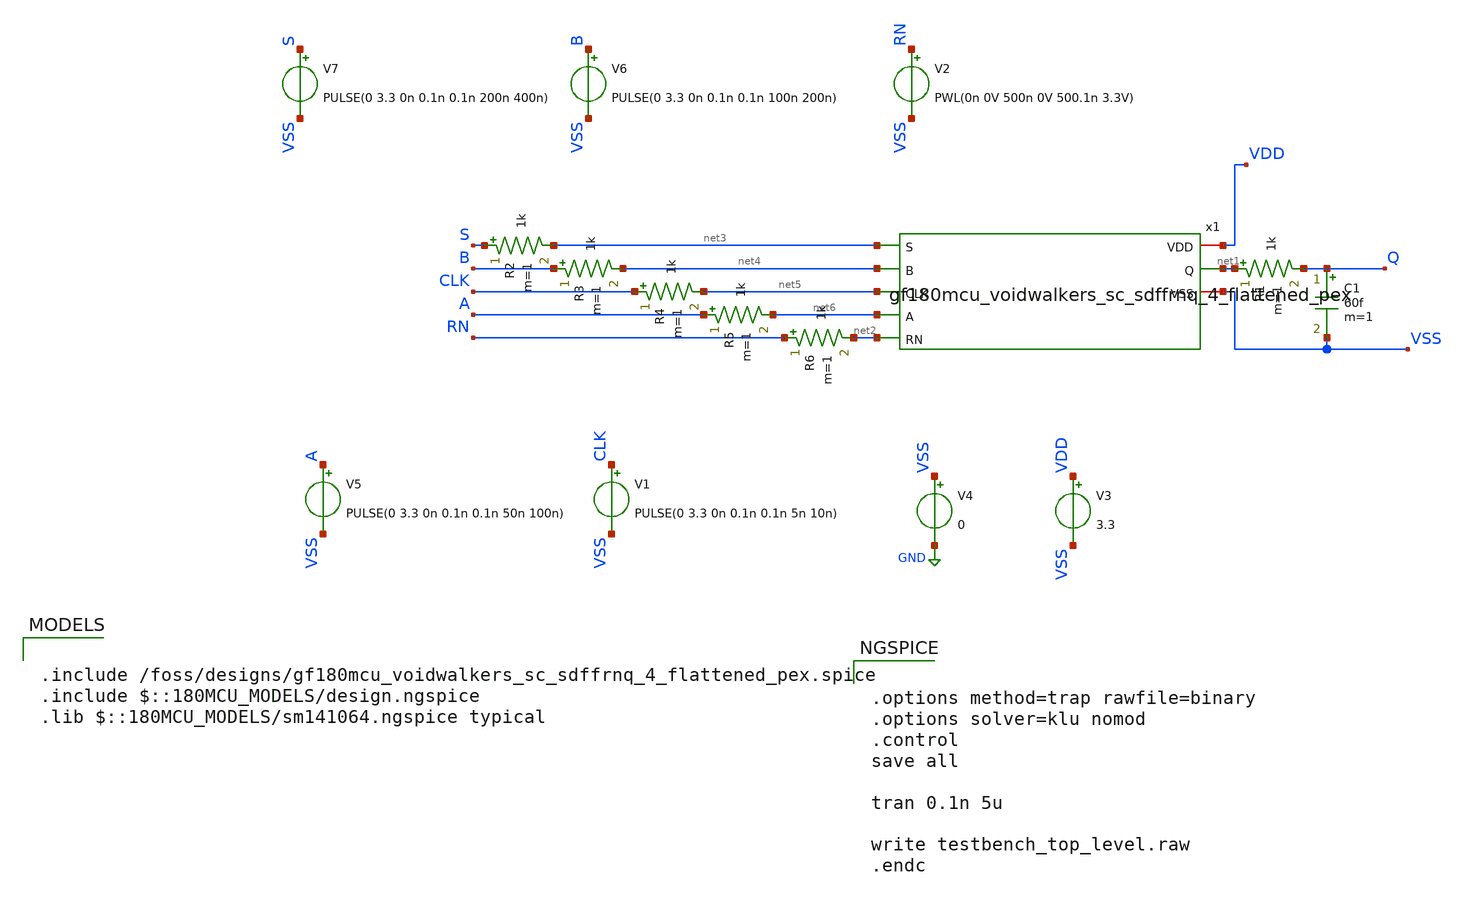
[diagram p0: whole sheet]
** sch_path: designs/libs/tb_digital/tb_toplevel/testbench_sdffrq_mux_tg.sch
**.subckt testbench_sdffrq_mux_tg
V1 CLK VSS PULSE(0 3.3 0n 0.1n 0.1n 5n 10n)
V3 VDD VSS 3.3
V4 VSS GND 0
V5 A VSS PULSE(0 3.3 0n 0.1n 0.1n 50n 100n)
V6 B VSS PULSE(0 3.3 0n 0.1n 0.1n 100n 200n)
V7 S VSS PULSE(0 3.3 0n 0.1n 0.1n 200n 400n)
V2 RN VSS PWL(0n 0V 500n 0V 500.1n 3.3V)
R1 net1 Q 1k m=1
R2 S net3 1k m=1
R3 B net4 1k m=1
R4 CLK net5 1k m=1
R5 A net6 1k m=1
R6 RN net2 1k m=1
x1 VDD VSS net6 net4 net3 net5 net2 net1 gf180mcu_voidwalkers_sc_sdffrnq_4_flattened_pex
C1 Q VSS 60f m=1
**** begin user architecture code

.include /foss/designs/gf180mcu_voidwalkers_sc_sdffrnq_4_flattened_pex.spice
.include $::180MCU_MODELS/design.ngspice
.lib $::180MCU_MODELS/sm141064.ngspice typical



.options method=trap rawfile=binary
.options solver=klu nomod
.control
save all

tran 0.1n 5u

write testbench_top_level.raw
.endc


**** end user architecture code
**.ends
.GLOBAL GND
.end
